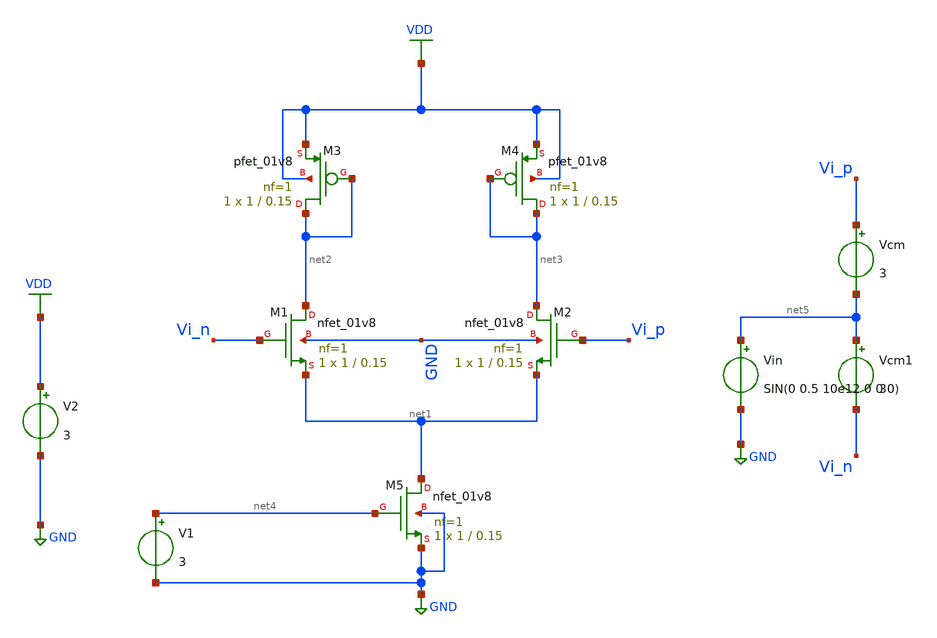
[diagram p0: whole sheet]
** sch_path: schem/amp.sch
**.subckt amp
XM2 net3 Vi_p net1 GND sky130_fd_pr__nfet_01v8 L=0.15 W=1 nf=1 ad='int((1 + 1)/2) * 1 / 1 * 0.29' as='int((1 + 2)/2) * 1 / 1 * 0.29'
+ pd='2*int((1 + 1)/2) * (1 / 1 + 0.29)' ps='2*int((1 + 2)/2) * (1 / 1 + 0.29)' nrd='0.29 / 1 ' nrs='0.29 / 1 '
+ sa=0 sb=0 sd=0 mult=1 m=1
XM3 net2 net2 VDD VDD sky130_fd_pr__pfet_01v8 L=0.15 W=1 nf=1 ad='int((1 + 1)/2) * 1 / 1 * 0.29' as='int((1 + 2)/2) * 1 / 1 * 0.29'
+ pd='2*int((1 + 1)/2) * (1 / 1 + 0.29)' ps='2*int((1 + 2)/2) * (1 / 1 + 0.29)' nrd='0.29 / 1 ' nrs='0.29 / 1 '
+ sa=0 sb=0 sd=0 mult=1 m=1
XM1 net2 Vi_n net1 GND sky130_fd_pr__nfet_01v8 L=0.15 W=1 nf=1 ad='int((1 + 1)/2) * 1 / 1 * 0.29' as='int((1 + 2)/2) * 1 / 1 * 0.29'
+ pd='2*int((1 + 1)/2) * (1 / 1 + 0.29)' ps='2*int((1 + 2)/2) * (1 / 1 + 0.29)' nrd='0.29 / 1 ' nrs='0.29 / 1 '
+ sa=0 sb=0 sd=0 mult=1 m=1
XM4 net3 net3 VDD VDD sky130_fd_pr__pfet_01v8 L=0.15 W=1 nf=1 ad='int((1 + 1)/2) * 1 / 1 * 0.29' as='int((1 + 2)/2) * 1 / 1 * 0.29'
+ pd='2*int((1 + 1)/2) * (1 / 1 + 0.29)' ps='2*int((1 + 2)/2) * (1 / 1 + 0.29)' nrd='0.29 / 1 ' nrs='0.29 / 1 '
+ sa=0 sb=0 sd=0 mult=1 m=1
XM5 net1 net4 GND GND sky130_fd_pr__nfet_01v8 L=0.15 W=1 nf=1 ad='int((1 + 1)/2) * 1 / 1 * 0.29' as='int((1 + 2)/2) * 1 / 1 * 0.29'
+ pd='2*int((1 + 1)/2) * (1 / 1 + 0.29)' ps='2*int((1 + 2)/2) * (1 / 1 + 0.29)' nrd='0.29 / 1 ' nrs='0.29 / 1 '
+ sa=0 sb=0 sd=0 mult=1 m=1
V1 net4 GND 3
Vcm Vi_p net5 3
Vin net5 GND SIN(0 0.5 10e12 0 0 0)
Vcm1 net5 Vi_n 3
V2 VDD GND 3
**** begin user architecture code

.control
    tran 1n 3n
    save all vi_p vi_n
    write amp.raw
.endc



** opencircuitdesign pdks install
.lib $::SKYWATER_MODELS/sky130.lib.spice tt

**** end user architecture code
**.ends
.GLOBAL VDD
.GLOBAL GND
.end
